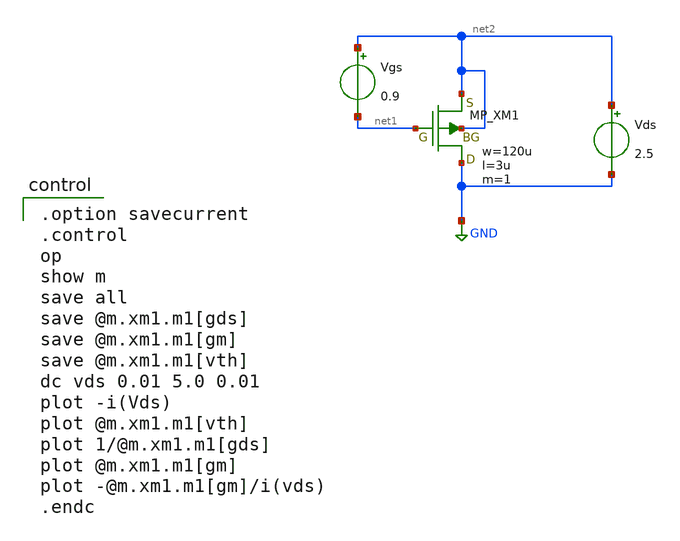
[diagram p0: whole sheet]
** sch_path: member_project/OPAMP/ShuntaroOhno/xschem/pmos_id_vds.sch
**.subckt pmos_id_vds
Vgs net2 net1 0.9
Vds net2 GND 2.5
XM1 GND net1 net2 net2 PMOS w=120u l=3u as=0 ad=0 ps=0 pd=0 nrd=0 nrs=0 m=1
**** begin user architecture code
 .include $::LIB/../ip62_models

.option savecurrent
.control
op
show m
save all
save @m.xm1.m1[gds]
save @m.xm1.m1[gm]
save @m.xm1.m1[vth]
dc vds 0.01 5.0 0.01
plot -i(Vds)
plot @m.xm1.m1[vth]
plot 1/@m.xm1.m1[gds]
plot @m.xm1.m1[gm]
plot -@m.xm1.m1[gm]/i(vds)
.endc

**** end user architecture code
**.ends
.GLOBAL GND
.end
